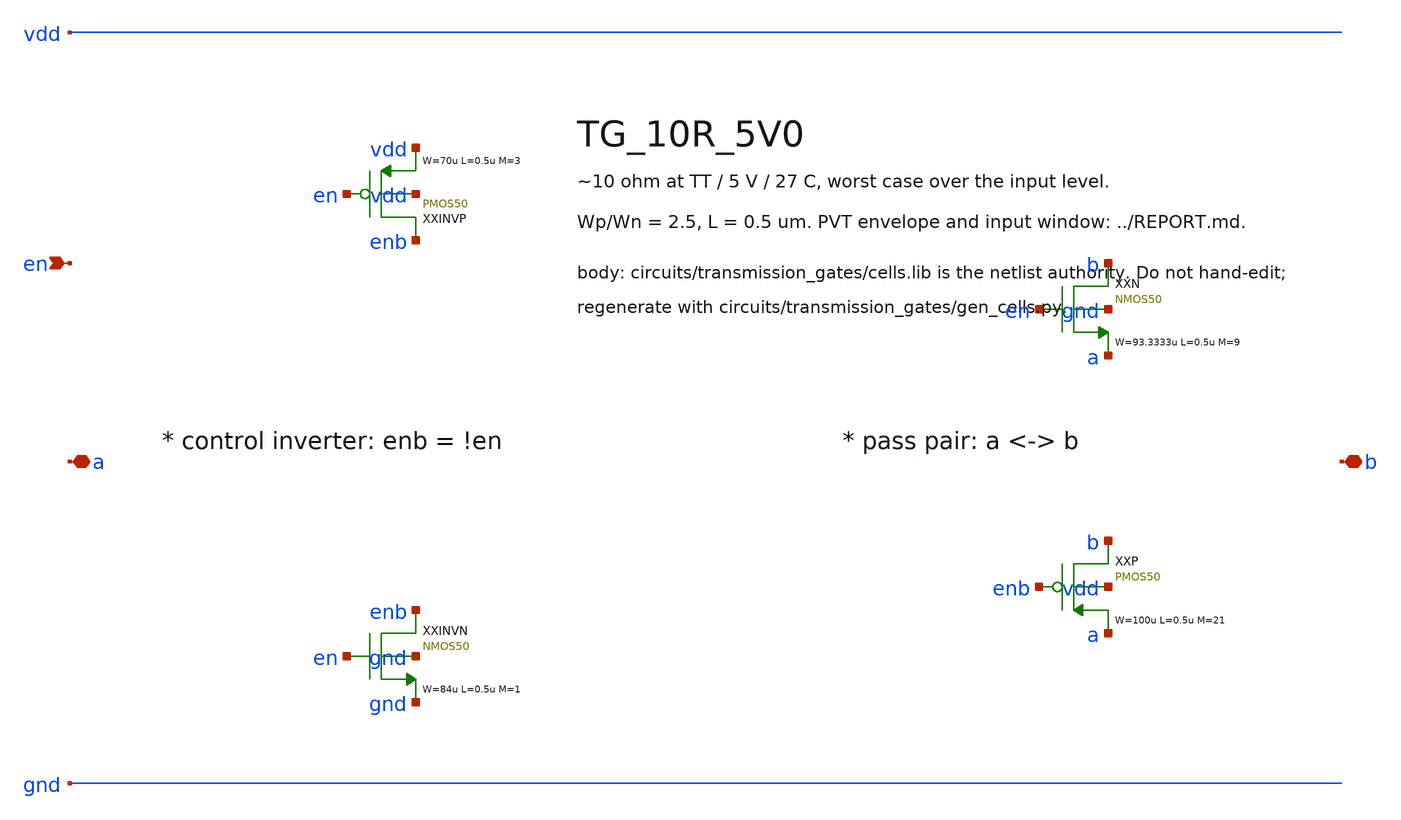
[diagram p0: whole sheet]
** sch_path: xschem/transmission_gates/TG_10R_5V0.sch
**.subckt TG_10R_5V0 a b en
*.iopin a
*.iopin b
*.ipin en
XXINVP enb en vdd vdd PMOS50 W=70u L=0.5u M=3 MM_SIGMA=0
XXINVN enb en gnd gnd NMOS50 W=84u L=0.5u M=1 MM_SIGMA=0
XXN b en a gnd NMOS50 W=93.3333u L=0.5u M=9 MM_SIGMA=0
XXP b enb a vdd PMOS50 W=100u L=0.5u M=21 MM_SIGMA=0
**.ends
.end
